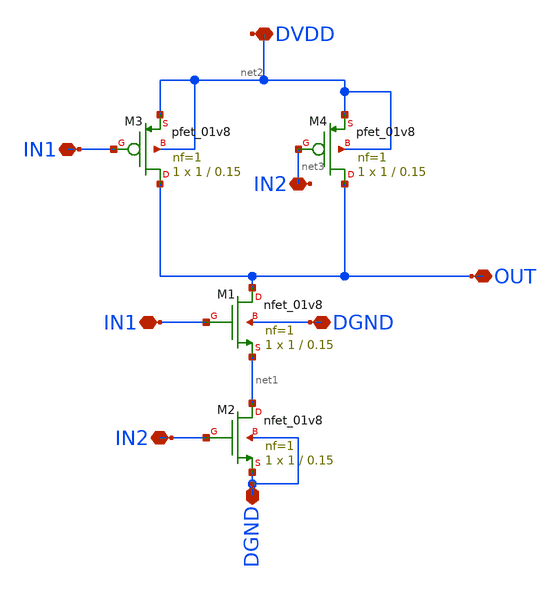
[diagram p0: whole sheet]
** sch_path: NAND2_eymenunay.sch
**.subckt NAND2_eymenunay IN1 IN1 IN2 IN2 OUT DVDD DGND DGND
*.iopin IN1
*.iopin IN1
*.iopin IN2
*.iopin IN2
*.iopin OUT
*.iopin DVDD
*.iopin DGND
*.iopin DGND
XM1 OUT IN1 net1 DGND sky130_fd_pr__nfet_01v8 L=0.15 W=1 nf=1 ad='int((nf+1)/2) * W/nf * 0.29' as='int((nf+2)/2) * W/nf * 0.29'
+ pd='2*int((nf+1)/2) * (W/nf + 0.29)' ps='2*int((nf+2)/2) * (W/nf + 0.29)' nrd='0.29 / W' nrs='0.29 / W'
+ sa=0 sb=0 sd=0 mult=1 m=1
XM2 net1 IN2 DGND DGND sky130_fd_pr__nfet_01v8 L=0.15 W=1 nf=1 ad='int((nf+1)/2) * W/nf * 0.29' as='int((nf+2)/2) * W/nf * 0.29'
+ pd='2*int((nf+1)/2) * (W/nf + 0.29)' ps='2*int((nf+2)/2) * (W/nf + 0.29)' nrd='0.29 / W' nrs='0.29 / W'
+ sa=0 sb=0 sd=0 mult=1 m=1
XM3 OUT IN1 net2 net2 sky130_fd_pr__pfet_01v8 L=0.15 W=1 nf=1 ad='int((nf+1)/2) * W/nf * 0.29' as='int((nf+2)/2) * W/nf * 0.29'
+ pd='2*int((nf+1)/2) * (W/nf + 0.29)' ps='2*int((nf+2)/2) * (W/nf + 0.29)' nrd='0.29 / W' nrs='0.29 / W'
+ sa=0 sb=0 sd=0 mult=1 m=1
XM4 OUT net3 net2 net2 sky130_fd_pr__pfet_01v8 L=0.15 W=1 nf=1 ad='int((nf+1)/2) * W/nf * 0.29' as='int((nf+2)/2) * W/nf * 0.29'
+ pd='2*int((nf+1)/2) * (W/nf + 0.29)' ps='2*int((nf+2)/2) * (W/nf + 0.29)' nrd='0.29 / W' nrs='0.29 / W'
+ sa=0 sb=0 sd=0 mult=1 m=1
**.ends
.end
